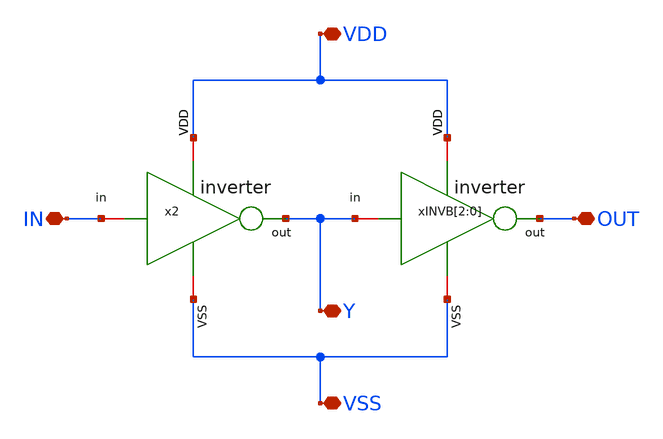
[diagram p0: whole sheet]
** sch_path: designs/sar_adc/digital/buffer_x1/xschem/buffer_VCB.sch
**.subckt buffer_VCB IN OUT VDD VSS Y
*.iopin IN
*.iopin OUT
*.iopin VDD
*.iopin VSS
*.iopin Y
x2 VDD IN Y VSS inverter
xINVB[2] VDD Y OUT VSS inverter
xINVB[1] VDD Y OUT VSS inverter
xINVB[0] VDD Y OUT VSS inverter
**.ends

* expanding   symbol:  designs/sar_adc/digital/inverter/xschem/inverter.sym # of pins=6
** sym_path: designs/sar_adc/digital/inverter/xschem/inverter.sym
** sch_path: designs/sar_adc/digital/inverter/xschem/inverter.sch
.subckt inverter VDD in out VSS
*.opin out
*.iopin in
*.iopin VDD
*.iopin VSS
XM1 out in VSS VSS nfet_03v3 L=0.28u W=1u nf=1 ad='int((nf+1)/2) * W/nf * 0.18u' as='int((nf+2)/2) * W/nf * 0.18u'
+ pd='2*int((nf+1)/2) * (W/nf + 0.18u)' ps='2*int((nf+2)/2) * (W/nf + 0.18u)' nrd='0.18u / W' nrs='0.18u / W'
+ sa=0 sb=0 sd=0 m=1
XM2 out in VDD VDD pfet_03v3 L=0.28u W=3u nf=1 ad='int((nf+1)/2) * W/nf * 0.18u' as='int((nf+2)/2) * W/nf * 0.18u'
+ pd='2*int((nf+1)/2) * (W/nf + 0.18u)' ps='2*int((nf+2)/2) * (W/nf + 0.18u)' nrd='0.18u / W' nrs='0.18u / W'
+ sa=0 sb=0 sd=0 m=1
.ends

.end
